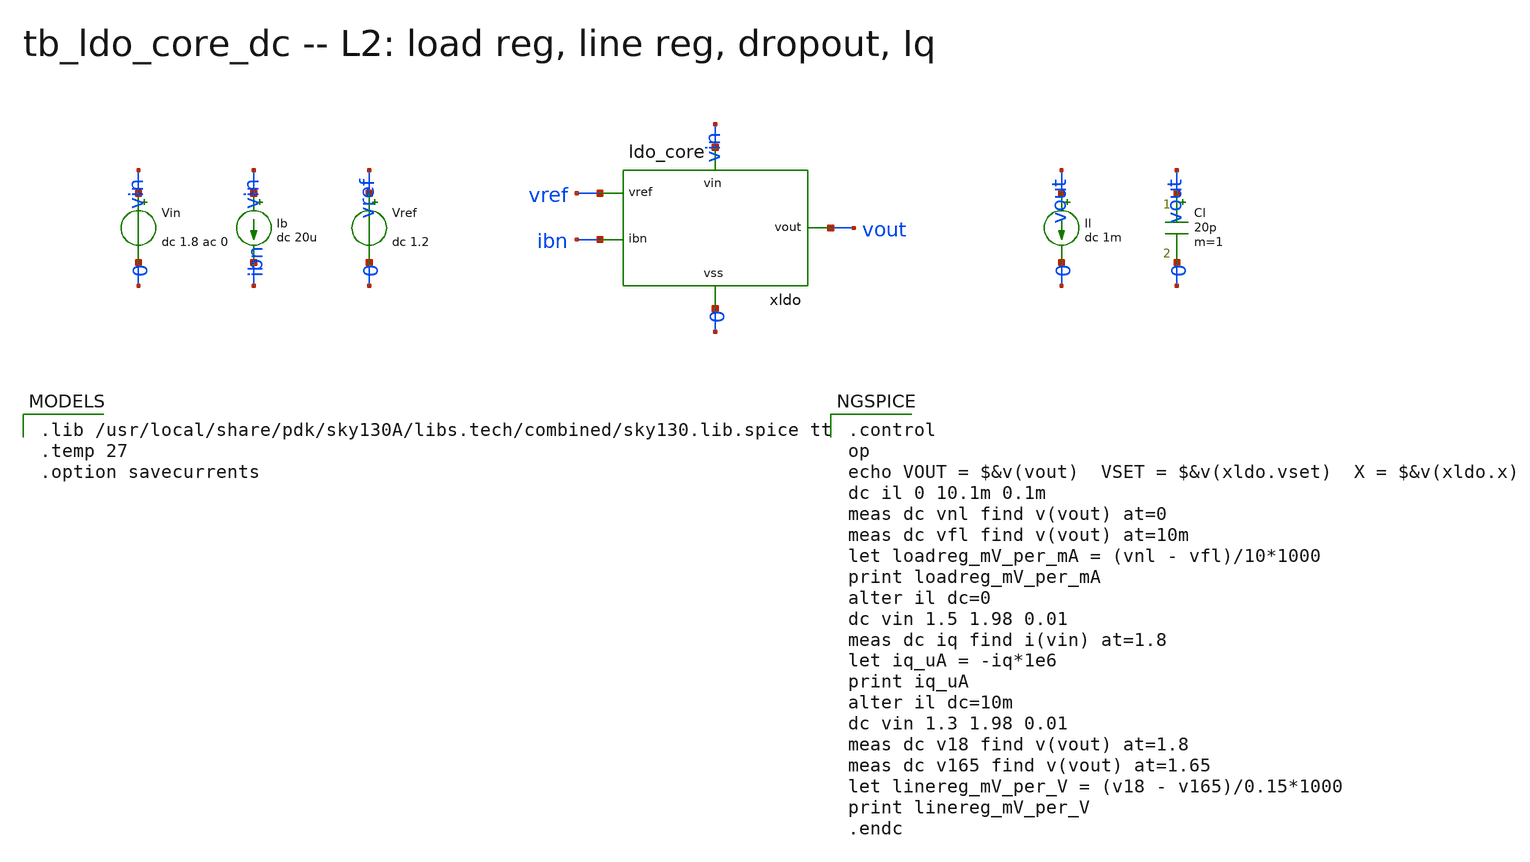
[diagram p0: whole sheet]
** sch_path: xschem/onetops_tb/tb_ldo_core_dc.sch
**.subckt tb_ldo_core_dc
Vin vin 0 dc 1.8 ac 0
Ib vin ibn dc 20u
Vref vref 0 dc 1.2
xldo vref ibn vout vin 0 ldo_core
Il vout 0 dc 1m
Cl vout 0 20p m=1
**** begin user architecture code

.lib /usr/local/share/pdk/sky130A/libs.tech/combined/sky130.lib.spice tt
.temp 27
.option savecurrents


.control
op
echo VOUT = $&v(vout)  VSET = $&v(xldo.vset)  X = $&v(xldo.x)
dc il 0 10.1m 0.1m
meas dc vnl find v(vout) at=0
meas dc vfl find v(vout) at=10m
let loadreg_mV_per_mA = (vnl - vfl)/10*1000
print loadreg_mV_per_mA
alter il dc=0
dc vin 1.5 1.98 0.01
meas dc iq find i(vin) at=1.8
let iq_uA = -iq*1e6
print iq_uA
alter il dc=10m
dc vin 1.3 1.98 0.01
meas dc v18 find v(vout) at=1.8
meas dc v165 find v(vout) at=1.65
let linereg_mV_per_V = (v18 - v165)/0.15*1000
print linereg_mV_per_V
.endc

**** end user architecture code
**.ends

* expanding   symbol:  onetops/ldo_core.sym # of pins=5
** sym_path: xschem/onetops/ldo_core.sym
** sch_path: xschem/onetops/ldo_core.sch
.subckt ldo_core vref ibn vout vin vss
*.ipin vref
*.ipin ibn
*.iopin vout
*.iopin vin
*.iopin vss
xbias ibn x vout i_pd i_tail vss bias_mirror
xvset vref i_pd i_tail vset vin vset_gen
xfvf vset x vout fvf_core
xprobe x xg lg_probe
xpass xg vout vin pass_pmos
xcomp x vout comp_rc
.ends


* expanding   symbol:  onetops/bias_mirror.sym # of pins=6
** sym_path: xschem/onetops/bias_mirror.sym
** sch_path: xschem/onetops/bias_mirror.sch
.subckt bias_mirror ibn o_fvf o_bl o_pd o_tail vss
*.ipin ibn
*.opin o_fvf
*.opin o_bl
*.opin o_pd
*.opin o_tail
*.iopin vss
XMN0 ibn ibn vss vss sky130_fd_pr__nfet_01v8 L=1 W=4 nf=1 ad='int((1 + 1)/2) * 4 / 1 * 0.29' as='int((1 + 2)/2) * 4 / 1 * 0.29'
+ pd='2*int((1 + 1)/2) * (4 / 1 + 0.29)' ps='2*int((1 + 2)/2) * (4 / 1 + 0.29)' nrd='0.29 / 4 ' nrs='0.29 / 4 '
+ sa=0 sb=0 sd=0 mult=1 m=1
XMN1 o_fvf ibn vss vss sky130_fd_pr__nfet_01v8 L=1 W=4 nf=1 ad='int((1 + 1)/2) * 4 / 1 * 0.29' as='int((1 + 2)/2) * 4 / 1 * 0.29'
+ pd='2*int((1 + 1)/2) * (4 / 1 + 0.29)' ps='2*int((1 + 2)/2) * (4 / 1 + 0.29)' nrd='0.29 / 4 ' nrs='0.29 / 4 '
+ sa=0 sb=0 sd=0 mult=1 m=1
XMN2 o_bl ibn vss vss sky130_fd_pr__nfet_01v8 L=1 W=4 nf=1 ad='int((1 + 1)/2) * 4 / 1 * 0.29' as='int((1 + 2)/2) * 4 / 1 * 0.29'
+ pd='2*int((1 + 1)/2) * (4 / 1 + 0.29)' ps='2*int((1 + 2)/2) * (4 / 1 + 0.29)' nrd='0.29 / 4 ' nrs='0.29 / 4 '
+ sa=0 sb=0 sd=0 mult=5 m=5
XMN3 o_pd ibn vss vss sky130_fd_pr__nfet_01v8 L=1 W=4 nf=1 ad='int((1 + 1)/2) * 4 / 1 * 0.29' as='int((1 + 2)/2) * 4 / 1 * 0.29'
+ pd='2*int((1 + 1)/2) * (4 / 1 + 0.29)' ps='2*int((1 + 2)/2) * (4 / 1 + 0.29)' nrd='0.29 / 4 ' nrs='0.29 / 4 '
+ sa=0 sb=0 sd=0 mult=1 m=1
XMN4 o_tail ibn vss vss sky130_fd_pr__nfet_01v8 L=1 W=4 nf=1 ad='int((1 + 1)/2) * 4 / 1 * 0.29' as='int((1 + 2)/2) * 4 / 1 * 0.29'
+ pd='2*int((1 + 1)/2) * (4 / 1 + 0.29)' ps='2*int((1 + 2)/2) * (4 / 1 + 0.29)' nrd='0.29 / 4 ' nrs='0.29 / 4 '
+ sa=0 sb=0 sd=0 mult=2 m=2
.ends


* expanding   symbol:  onetops/vset_gen.sym # of pins=5
** sym_path: xschem/onetops/vset_gen.sym
** sch_path: xschem/onetops/vset_gen.sch
.subckt vset_gen vref i_pd i_tail vset vin
*.ipin vref
*.opin vset
*.iopin i_pd
*.iopin i_tail
*.iopin vin
XMPD i_pd i_pd vin vin sky130_fd_pr__pfet_01v8_lvt L=2 W=10 nf=1 ad='int((1 + 1)/2) * 10 / 1 * 0.29'
+ as='int((1 + 2)/2) * 10 / 1 * 0.29' pd='2*int((1 + 1)/2) * (10 / 1 + 0.29)' ps='2*int((1 + 2)/2) * (10 / 1 + 0.29)'
+ nrd='0.29 / 10 ' nrs='0.29 / 10 ' sa=0 sb=0 sd=0 mult=1 m=1
XMPS vrep i_pd vin vin sky130_fd_pr__pfet_01v8_lvt L=2 W=10 nf=1 ad='int((1 + 1)/2) * 10 / 1 * 0.29'
+ as='int((1 + 2)/2) * 10 / 1 * 0.29' pd='2*int((1 + 1)/2) * (10 / 1 + 0.29)' ps='2*int((1 + 2)/2) * (10 / 1 + 0.29)'
+ nrd='0.29 / 10 ' nrs='0.29 / 10 ' sa=0 sb=0 sd=0 mult=1 m=1
XMR 0 vset vrep vrep sky130_fd_pr__pfet_01v8_lvt L=1 W=100 nf=1 ad='int((1 + 1)/2) * 100 / 1 * 0.29'
+ as='int((1 + 2)/2) * 100 / 1 * 0.29' pd='2*int((1 + 1)/2) * (100 / 1 + 0.29)' ps='2*int((1 + 2)/2) * (100 / 1 + 0.29)'
+ nrd='0.29 / 100 ' nrs='0.29 / 100 ' sa=0 sb=0 sd=0 mult=1 m=1
xota vref vrep i_tail vset vin ota5t
Cset vset 0 2p m=1
.ends


* expanding   symbol:  onetops/fvf_core.sym # of pins=3
** sym_path: xschem/onetops/fvf_core.sym
** sch_path: xschem/onetops/fvf_core.sch
.subckt fvf_core vset x vout
*.ipin vset
*.opin x
*.iopin vout
XMC x vset vout vout sky130_fd_pr__pfet_01v8_lvt L=1 W=100 nf=1 ad='int((1 + 1)/2) * 100 / 1 * 0.29'
+ as='int((1 + 2)/2) * 100 / 1 * 0.29' pd='2*int((1 + 1)/2) * (100 / 1 + 0.29)' ps='2*int((1 + 2)/2) * (100 / 1 + 0.29)'
+ nrd='0.29 / 100 ' nrs='0.29 / 100 ' sa=0 sb=0 sd=0 mult=1 m=1
.ends


* expanding   symbol:  onetops/lg_probe.sym # of pins=2
** sym_path: xschem/onetops/lg_probe.sym
** sch_path: xschem/onetops/lg_probe.sch
.subckt lg_probe drv lin
*.iopin drv
*.iopin lin
Vbrk lin drv dc 0 ac 0
Iinj 0 lin dc 0 ac 0
.ends


* expanding   symbol:  onetops/pass_pmos.sym # of pins=3
** sym_path: xschem/onetops/pass_pmos.sym
** sch_path: xschem/onetops/pass_pmos.sch
.subckt pass_pmos g vout vin
*.ipin g
*.iopin vin
*.iopin vout
XMP vout g vin vin sky130_fd_pr__pfet_01v8 L=0.35 W=10 nf=1 ad='int((1 + 1)/2) * 10 / 1 * 0.29' as='int((1 + 2)/2) * 10 / 1 * 0.29'
+ pd='2*int((1 + 1)/2) * (10 / 1 + 0.29)' ps='2*int((1 + 2)/2) * (10 / 1 + 0.29)' nrd='0.29 / 10 ' nrs='0.29 / 10 '
+ sa=0 sb=0 sd=0 mult=70 m=70
.ends


* expanding   symbol:  onetops/comp_rc.sym # of pins=2
** sym_path: xschem/onetops/comp_rc.sym
** sch_path: xschem/onetops/comp_rc.sch
.subckt comp_rc a b
*.iopin a
*.iopin b
Rz a n1 1 m=1
Cc n1 b 4p m=1
.ends


* expanding   symbol:  onetops/ota5t.sym # of pins=5
** sym_path: xschem/onetops/ota5t.sym
** sch_path: xschem/onetops/ota5t.sch
.subckt ota5t inp inn tail out vdd
*.ipin inp
*.ipin inn
*.opin out
*.iopin tail
*.iopin vdd
XMP1 nd nd vdd vdd sky130_fd_pr__pfet_01v8_lvt L=2 W=20 nf=1 ad='int((1 + 1)/2) * 20 / 1 * 0.29' as='int((1 + 2)/2) * 20 / 1 * 0.29'
+ pd='2*int((1 + 1)/2) * (20 / 1 + 0.29)' ps='2*int((1 + 2)/2) * (20 / 1 + 0.29)' nrd='0.29 / 20 ' nrs='0.29 / 20 '
+ sa=0 sb=0 sd=0 mult=1 m=1
XMP2 out nd vdd vdd sky130_fd_pr__pfet_01v8_lvt L=2 W=20 nf=1 ad='int((1 + 1)/2) * 20 / 1 * 0.29' as='int((1 + 2)/2) * 20 / 1 * 0.29'
+ pd='2*int((1 + 1)/2) * (20 / 1 + 0.29)' ps='2*int((1 + 2)/2) * (20 / 1 + 0.29)' nrd='0.29 / 20 ' nrs='0.29 / 20 '
+ sa=0 sb=0 sd=0 mult=1 m=1
XMN1 nd inp tail 0 sky130_fd_pr__nfet_01v8 L=1 W=5 nf=1 ad='int((1 + 1)/2) * 5 / 1 * 0.29' as='int((1 + 2)/2) * 5 / 1 * 0.29'
+ pd='2*int((1 + 1)/2) * (5 / 1 + 0.29)' ps='2*int((1 + 2)/2) * (5 / 1 + 0.29)' nrd='0.29 / 5 ' nrs='0.29 / 5 '
+ sa=0 sb=0 sd=0 mult=1 m=1
XMN2 out inn tail 0 sky130_fd_pr__nfet_01v8 L=1 W=5 nf=1 ad='int((1 + 1)/2) * 5 / 1 * 0.29' as='int((1 + 2)/2) * 5 / 1 * 0.29'
+ pd='2*int((1 + 1)/2) * (5 / 1 + 0.29)' ps='2*int((1 + 2)/2) * (5 / 1 + 0.29)' nrd='0.29 / 5 ' nrs='0.29 / 5 '
+ sa=0 sb=0 sd=0 mult=1 m=1
.ends

.end
